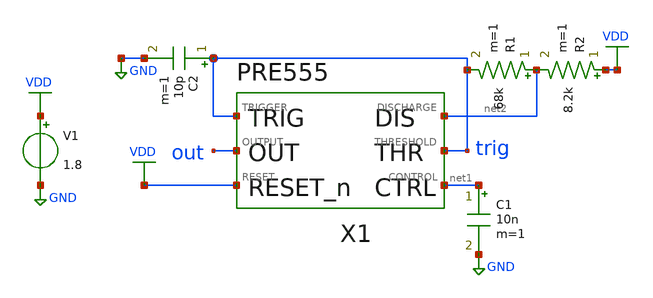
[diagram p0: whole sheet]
** sch_path: xschem/astable_tb.sch
**.subckt astable_tb
X1 trig out VDD trig net2 net1 pre555
V1 VDD GND 1.8
C1 net1 GND 10n m=1
R1 net2 trig 68k m=1
R2 VDD net2 8.2k m=1
C2 trig GND 10p m=1
**** begin user architecture code


.option wnflag=1
.lib /usr/local/share/pdk/sky130A/libs.tech/ngspice/sky130.lib.spice tt
.tran 0.01u 100u


**** end user architecture code
**.ends

* expanding   symbol:  pre555.sym # of pins=6
** sym_path: xschem/pre555.sym
** sch_path: xschem/pre555.sch
.subckt pre555 TRIGGER OUTPUT RESET THRESHOLD DISCHARGE CONTROL
*.iopin DISCHARGE
*.ipin TRIGGER
*.ipin THRESHOLD
*.ipin CONTROL
*.ipin RESET
*.opin OUTPUT
X1 net1 CONTROL vdiv
X2 THRESHOLD CONTROL net3 comp
X3 net1 TRIGGER net2 comp
X4 net2 net3 net4 net5 sr_latch
X5 RESET net5 inverter
XM2 DISCHARGE net6 GND GND sky130_fd_pr__nfet_01v8 L=0.15 W=12 nf=1 ad='int((1 + 1)/2) * 12 / 1 * 0.29'
+ as='int((1 + 2)/2) * 12 / 1 * 0.29' pd='2*int((1 + 1)/2) * (12 / 1 + 0.29)' ps='2*int((1 + 2)/2) * (12 / 1 + 0.29)'
+ nrd='0.29 / 12 ' nrs='0.29 / 12 ' sa=0 sb=0 sd=0 mult=6 m=6
X6 net4 net6 inverter
X7 net6 OUTPUT inverter
.ends


* expanding   symbol:  vdiv.sym # of pins=2
** sym_path: xschem/vdiv.sym
** sch_path: xschem/vdiv.sch
.subckt vdiv v1t v2t
*.iopin v2t
*.iopin v1t
XR1 v2t VDD res100k
XR2 v1t v2t res100k
XR3 GND v1t res100k
.ends


* expanding   symbol:  comp.sym # of pins=3
** sym_path: xschem/comp.sym
** sch_path: xschem/comp.sch
.subckt comp inp inn out
*.ipin inp
*.ipin inn
*.opin out
XM1 net1 inn net3 GND sky130_fd_pr__nfet_01v8 L=1 W=1 nf=1 ad='int((1 + 1)/2) * 1 / 1 * 0.29' as='int((1 + 2)/2) * 1 / 1 * 0.29'
+ pd='2*int((1 + 1)/2) * (1 / 1 + 0.29)' ps='2*int((1 + 2)/2) * (1 / 1 + 0.29)' nrd='0.29 / 1 ' nrs='0.29 / 1 '
+ sa=0 sb=0 sd=0 mult=1 m=1
XM2 net1 net1 VDD VDD sky130_fd_pr__pfet_01v8 L=1 W=1 nf=1 ad='int((1 + 1)/2) * 1 / 1 * 0.29' as='int((1 + 2)/2) * 1 / 1 * 0.29'
+ pd='2*int((1 + 1)/2) * (1 / 1 + 0.29)' ps='2*int((1 + 2)/2) * (1 / 1 + 0.29)' nrd='0.29 / 1 ' nrs='0.29 / 1 '
+ sa=0 sb=0 sd=0 mult=1 m=1
XM3 net2 net1 VDD VDD sky130_fd_pr__pfet_01v8 L=1 W=1 nf=1 ad='int((1 + 1)/2) * 1 / 1 * 0.29' as='int((1 + 2)/2) * 1 / 1 * 0.29'
+ pd='2*int((1 + 1)/2) * (1 / 1 + 0.29)' ps='2*int((1 + 2)/2) * (1 / 1 + 0.29)' nrd='0.29 / 1 ' nrs='0.29 / 1 '
+ sa=0 sb=0 sd=0 mult=1 m=1
XM4 net2 inp net3 GND sky130_fd_pr__nfet_01v8 L=1 W=1 nf=1 ad='int((1 + 1)/2) * 1 / 1 * 0.29' as='int((1 + 2)/2) * 1 / 1 * 0.29'
+ pd='2*int((1 + 1)/2) * (1 / 1 + 0.29)' ps='2*int((1 + 2)/2) * (1 / 1 + 0.29)' nrd='0.29 / 1 ' nrs='0.29 / 1 '
+ sa=0 sb=0 sd=0 mult=1 m=1
XM5 net3 net4 GND GND sky130_fd_pr__nfet_01v8 L=1 W=3.5 nf=1 ad='int((1 + 1)/2) * 3.5 / 1 * 0.29' as='int((1 + 2)/2) * 3.5 / 1 * 0.29'
+ pd='2*int((1 + 1)/2) * (3.5 / 1 + 0.29)' ps='2*int((1 + 2)/2) * (3.5 / 1 + 0.29)' nrd='0.29 / 3.5 ' nrs='0.29 / 3.5 '
+ sa=0 sb=0 sd=0 mult=1 m=1
XM6 net4 net4 GND GND sky130_fd_pr__nfet_01v8 L=1 W=3.5 nf=1 ad='int((1 + 1)/2) * 3.5 / 1 * 0.29' as='int((1 + 2)/2) * 3.5 / 1 * 0.29'
+ pd='2*int((1 + 1)/2) * (3.5 / 1 + 0.29)' ps='2*int((1 + 2)/2) * (3.5 / 1 + 0.29)' nrd='0.29 / 3.5 ' nrs='0.29 / 3.5 '
+ sa=0 sb=0 sd=0 mult=1 m=1
XR1 net4 VDD res100k
X1 net2 out inverter
.ends


* expanding   symbol:  sr_latch.sym # of pins=4
** sym_path: xschem/sr_latch.sym
** sch_path: xschem/sr_latch.sch
.subckt sr_latch s r0 q r1
*.ipin s
*.ipin r0
*.opin q
*.ipin r1
XM1 net1 q net2 VDD sky130_fd_pr__pfet_01v8 L=0.15 W=1 nf=1 ad='int((1 + 1)/2) * 1 / 1 * 0.29' as='int((1 + 2)/2) * 1 / 1 * 0.29'
+ pd='2*int((1 + 1)/2) * (1 / 1 + 0.29)' ps='2*int((1 + 2)/2) * (1 / 1 + 0.29)' nrd='0.29 / 1 ' nrs='0.29 / 1 '
+ sa=0 sb=0 sd=0 mult=1 m=1
XM2 net2 s VDD VDD sky130_fd_pr__pfet_01v8 L=0.15 W=1 nf=1 ad='int((1 + 1)/2) * 1 / 1 * 0.29' as='int((1 + 2)/2) * 1 / 1 * 0.29'
+ pd='2*int((1 + 1)/2) * (1 / 1 + 0.29)' ps='2*int((1 + 2)/2) * (1 / 1 + 0.29)' nrd='0.29 / 1 ' nrs='0.29 / 1 '
+ sa=0 sb=0 sd=0 mult=1 m=1
XM3 net1 s GND GND sky130_fd_pr__nfet_01v8 L=0.15 W=1 nf=1 ad='int((1 + 1)/2) * 1 / 1 * 0.29' as='int((1 + 2)/2) * 1 / 1 * 0.29'
+ pd='2*int((1 + 1)/2) * (1 / 1 + 0.29)' ps='2*int((1 + 2)/2) * (1 / 1 + 0.29)' nrd='0.29 / 1 ' nrs='0.29 / 1 '
+ sa=0 sb=0 sd=0 mult=1 m=1
XM4 net1 q GND GND sky130_fd_pr__nfet_01v8 L=0.15 W=1 nf=1 ad='int((1 + 1)/2) * 1 / 1 * 0.29' as='int((1 + 2)/2) * 1 / 1 * 0.29'
+ pd='2*int((1 + 1)/2) * (1 / 1 + 0.29)' ps='2*int((1 + 2)/2) * (1 / 1 + 0.29)' nrd='0.29 / 1 ' nrs='0.29 / 1 '
+ sa=0 sb=0 sd=0 mult=1 m=1
XM5 q net1 net3 VDD sky130_fd_pr__pfet_01v8 L=0.15 W=1 nf=1 ad='int((1 + 1)/2) * 1 / 1 * 0.29' as='int((1 + 2)/2) * 1 / 1 * 0.29'
+ pd='2*int((1 + 1)/2) * (1 / 1 + 0.29)' ps='2*int((1 + 2)/2) * (1 / 1 + 0.29)' nrd='0.29 / 1 ' nrs='0.29 / 1 '
+ sa=0 sb=0 sd=0 mult=1 m=1
XM6 net3 r0 net4 VDD sky130_fd_pr__pfet_01v8 L=0.15 W=1 nf=1 ad='int((1 + 1)/2) * 1 / 1 * 0.29' as='int((1 + 2)/2) * 1 / 1 * 0.29'
+ pd='2*int((1 + 1)/2) * (1 / 1 + 0.29)' ps='2*int((1 + 2)/2) * (1 / 1 + 0.29)' nrd='0.29 / 1 ' nrs='0.29 / 1 '
+ sa=0 sb=0 sd=0 mult=1 m=1
XM7 q r0 GND GND sky130_fd_pr__nfet_01v8 L=0.15 W=1 nf=1 ad='int((1 + 1)/2) * 1 / 1 * 0.29' as='int((1 + 2)/2) * 1 / 1 * 0.29'
+ pd='2*int((1 + 1)/2) * (1 / 1 + 0.29)' ps='2*int((1 + 2)/2) * (1 / 1 + 0.29)' nrd='0.29 / 1 ' nrs='0.29 / 1 '
+ sa=0 sb=0 sd=0 mult=1 m=1
XM8 q net1 GND GND sky130_fd_pr__nfet_01v8 L=0.15 W=1 nf=1 ad='int((1 + 1)/2) * 1 / 1 * 0.29' as='int((1 + 2)/2) * 1 / 1 * 0.29'
+ pd='2*int((1 + 1)/2) * (1 / 1 + 0.29)' ps='2*int((1 + 2)/2) * (1 / 1 + 0.29)' nrd='0.29 / 1 ' nrs='0.29 / 1 '
+ sa=0 sb=0 sd=0 mult=1 m=1
XM9 net4 r1 VDD VDD sky130_fd_pr__pfet_01v8 L=0.15 W=1 nf=1 ad='int((1 + 1)/2) * 1 / 1 * 0.29' as='int((1 + 2)/2) * 1 / 1 * 0.29'
+ pd='2*int((1 + 1)/2) * (1 / 1 + 0.29)' ps='2*int((1 + 2)/2) * (1 / 1 + 0.29)' nrd='0.29 / 1 ' nrs='0.29 / 1 '
+ sa=0 sb=0 sd=0 mult=1 m=1
XM10 q r1 GND GND sky130_fd_pr__nfet_01v8 L=0.15 W=1 nf=1 ad='int((1 + 1)/2) * 1 / 1 * 0.29' as='int((1 + 2)/2) * 1 / 1 * 0.29'
+ pd='2*int((1 + 1)/2) * (1 / 1 + 0.29)' ps='2*int((1 + 2)/2) * (1 / 1 + 0.29)' nrd='0.29 / 1 ' nrs='0.29 / 1 '
+ sa=0 sb=0 sd=0 mult=1 m=1
.ends


* expanding   symbol:  inverter.sym # of pins=2
** sym_path: xschem/inverter.sym
** sch_path: xschem/inverter.sch
.subckt inverter a y
*.ipin a
*.opin y
XM1 y a GND GND sky130_fd_pr__nfet_01v8 L=0.15 W=1 nf=1 ad='int((1 + 1)/2) * 1 / 1 * 0.29' as='int((1 + 2)/2) * 1 / 1 * 0.29'
+ pd='2*int((1 + 1)/2) * (1 / 1 + 0.29)' ps='2*int((1 + 2)/2) * (1 / 1 + 0.29)' nrd='0.29 / 1 ' nrs='0.29 / 1 '
+ sa=0 sb=0 sd=0 mult=1 m=1
XM2 y a VDD VDD sky130_fd_pr__pfet_01v8 L=0.15 W=1 nf=1 ad='int((1 + 1)/2) * 1 / 1 * 0.29' as='int((1 + 2)/2) * 1 / 1 * 0.29'
+ pd='2*int((1 + 1)/2) * (1 / 1 + 0.29)' ps='2*int((1 + 2)/2) * (1 / 1 + 0.29)' nrd='0.29 / 1 ' nrs='0.29 / 1 '
+ sa=0 sb=0 sd=0 mult=1 m=1
.ends


* expanding   symbol:  res100k.sym # of pins=2
** sym_path: xschem/res100k.sym
** sch_path: xschem/res100k.sch
.subckt res100k bot top
*.iopin top
*.iopin bot
XR1 net1 top GND sky130_fd_pr__res_xhigh_po_0p35 L=3.5 mult=1 m=1
XR2 net2 net1 GND sky130_fd_pr__res_xhigh_po_0p35 L=3.5 mult=1 m=1
XR3 net3 net2 GND sky130_fd_pr__res_xhigh_po_0p35 L=3.5 mult=1 m=1
XR4 net4 net3 GND sky130_fd_pr__res_xhigh_po_0p35 L=3.5 mult=1 m=1
XR5 bot net4 GND sky130_fd_pr__res_xhigh_po_0p35 L=3.5 mult=1 m=1
.ends

.GLOBAL VDD
.GLOBAL GND
.end
